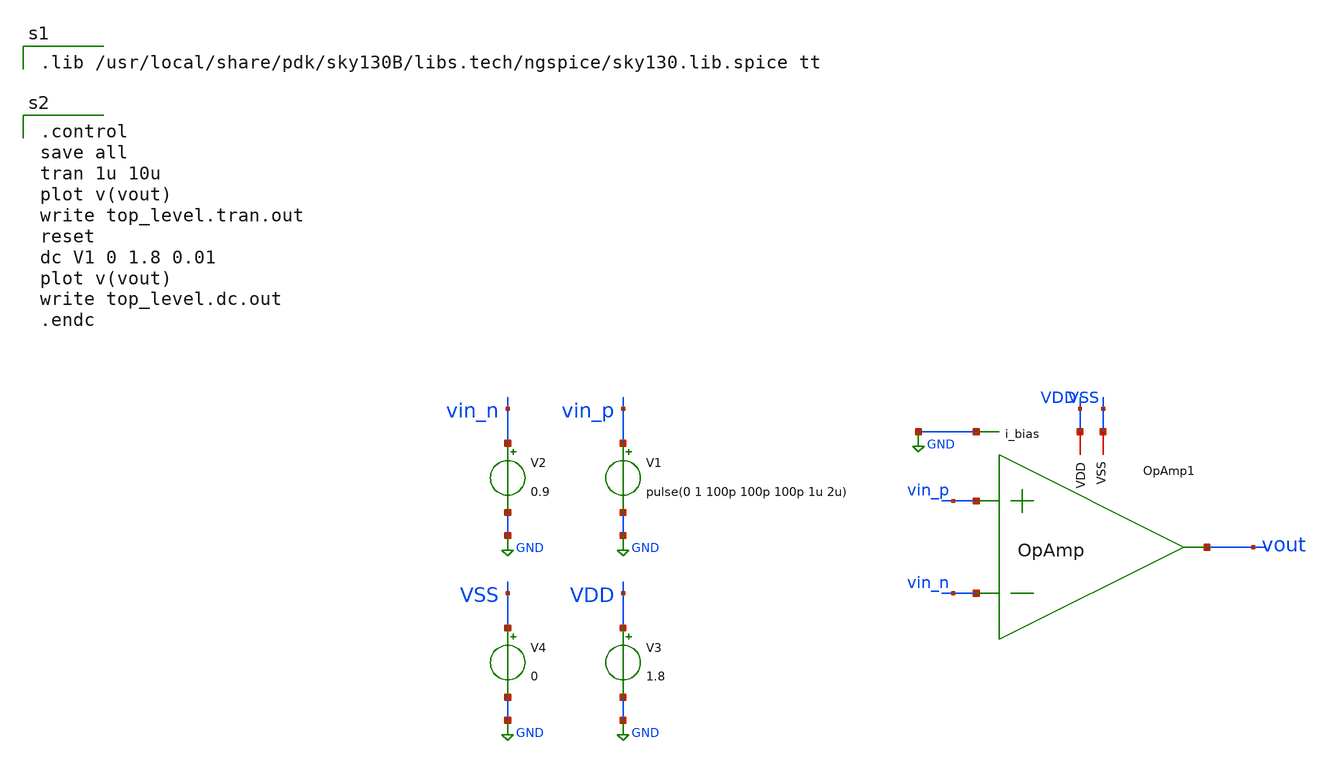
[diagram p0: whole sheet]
** sch_path: ISSCC_2025_V1/xschem/TB/top_level.sch
**.subckt top_level
V1 vin_p GND pulse(0 1 100p 100p 100p 1u 2u)
V2 vin_n GND 0.9
V3 VDD GND 1.8
OpAmp1 VDD vout vin_p vin_n VSS GND OpAmp
V4 VSS GND 0
**** begin user architecture code

.lib /usr/local/share/pdk/sky130B/libs.tech/ngspice/sky130.lib.spice tt


.control
save all
tran 1u 10u
plot v(vout)
write top_level.tran.out
reset
dc V1 0 1.8 0.01
plot v(vout)
write top_level.dc.out
.endc

**** end user architecture code
**.ends

* expanding   symbol:  Benchmark_Circuits/OpAmp/OpAmp.sym # of pins=6
** sym_path: ISSCC_2025_V1/xschem/Benchmark_Circuits/OpAmp/OpAmp.sym
** sch_path: ISSCC_2025_V1/xschem/Benchmark_Circuits/OpAmp/OpAmp.sch
.subckt OpAmp VDD vout vin_p vin_n VSS i_bias
*.ipin vin_p
*.ipin vin_n
*.iopin VSS
*.iopin VDD
*.opin vout
*.ipin i_bias
XM1 net2 vin_p net1 VSS sky130_fd_pr__nfet_01v8 L=2 W=4 nf=1 ad='int((nf+1)/2) * W/nf * 0.29' as='int((nf+2)/2) * W/nf * 0.29'
+ pd='2*int((nf+1)/2) * (W/nf + 0.29)' ps='2*int((nf+2)/2) * (W/nf + 0.29)' nrd='0.29 / W' nrs='0.29 / W'
+ sa=0 sb=0 sd=0 mult=1 m=1
XM2 vout vin_n net1 VSS sky130_fd_pr__nfet_01v8 L=2 W=4 nf=1 ad='int((nf+1)/2) * W/nf * 0.29' as='int((nf+2)/2) * W/nf * 0.29'
+ pd='2*int((nf+1)/2) * (W/nf + 0.29)' ps='2*int((nf+2)/2) * (W/nf + 0.29)' nrd='0.29 / W' nrs='0.29 / W'
+ sa=0 sb=0 sd=0 mult=1 m=1
XM3 net1 i_bias VSS VSS sky130_fd_pr__nfet_01v8 L=2 W=4 nf=1 ad='int((nf+1)/2) * W/nf * 0.29' as='int((nf+2)/2) * W/nf * 0.29'
+ pd='2*int((nf+1)/2) * (W/nf + 0.29)' ps='2*int((nf+2)/2) * (W/nf + 0.29)' nrd='0.29 / W' nrs='0.29 / W'
+ sa=0 sb=0 sd=0 mult=1 m=1
XM6 i_bias i_bias VSS VSS sky130_fd_pr__nfet_01v8 L=2 W=4 nf=1 ad='int((nf+1)/2) * W/nf * 0.29' as='int((nf+2)/2) * W/nf * 0.29'
+ pd='2*int((nf+1)/2) * (W/nf + 0.29)' ps='2*int((nf+2)/2) * (W/nf + 0.29)' nrd='0.29 / W' nrs='0.29 / W'
+ sa=0 sb=0 sd=0 mult=1 m=1
XM4 vout net2 VDD VDD sky130_fd_pr__pfet_01v8 L=2 W=4 nf=1 ad='int((nf+1)/2) * W/nf * 0.29' as='int((nf+2)/2) * W/nf * 0.29'
+ pd='2*int((nf+1)/2) * (W/nf + 0.29)' ps='2*int((nf+2)/2) * (W/nf + 0.29)' nrd='0.29 / W' nrs='0.29 / W'
+ sa=0 sb=0 sd=0 mult=1 m=1
XM5 net2 net2 VDD VDD sky130_fd_pr__pfet_01v8 L=2 W=4 nf=1 ad='int((nf+1)/2) * W/nf * 0.29' as='int((nf+2)/2) * W/nf * 0.29'
+ pd='2*int((nf+1)/2) * (W/nf + 0.29)' ps='2*int((nf+2)/2) * (W/nf + 0.29)' nrd='0.29 / W' nrs='0.29 / W'
+ sa=0 sb=0 sd=0 mult=1 m=1
.ends

.GLOBAL GND
.end
